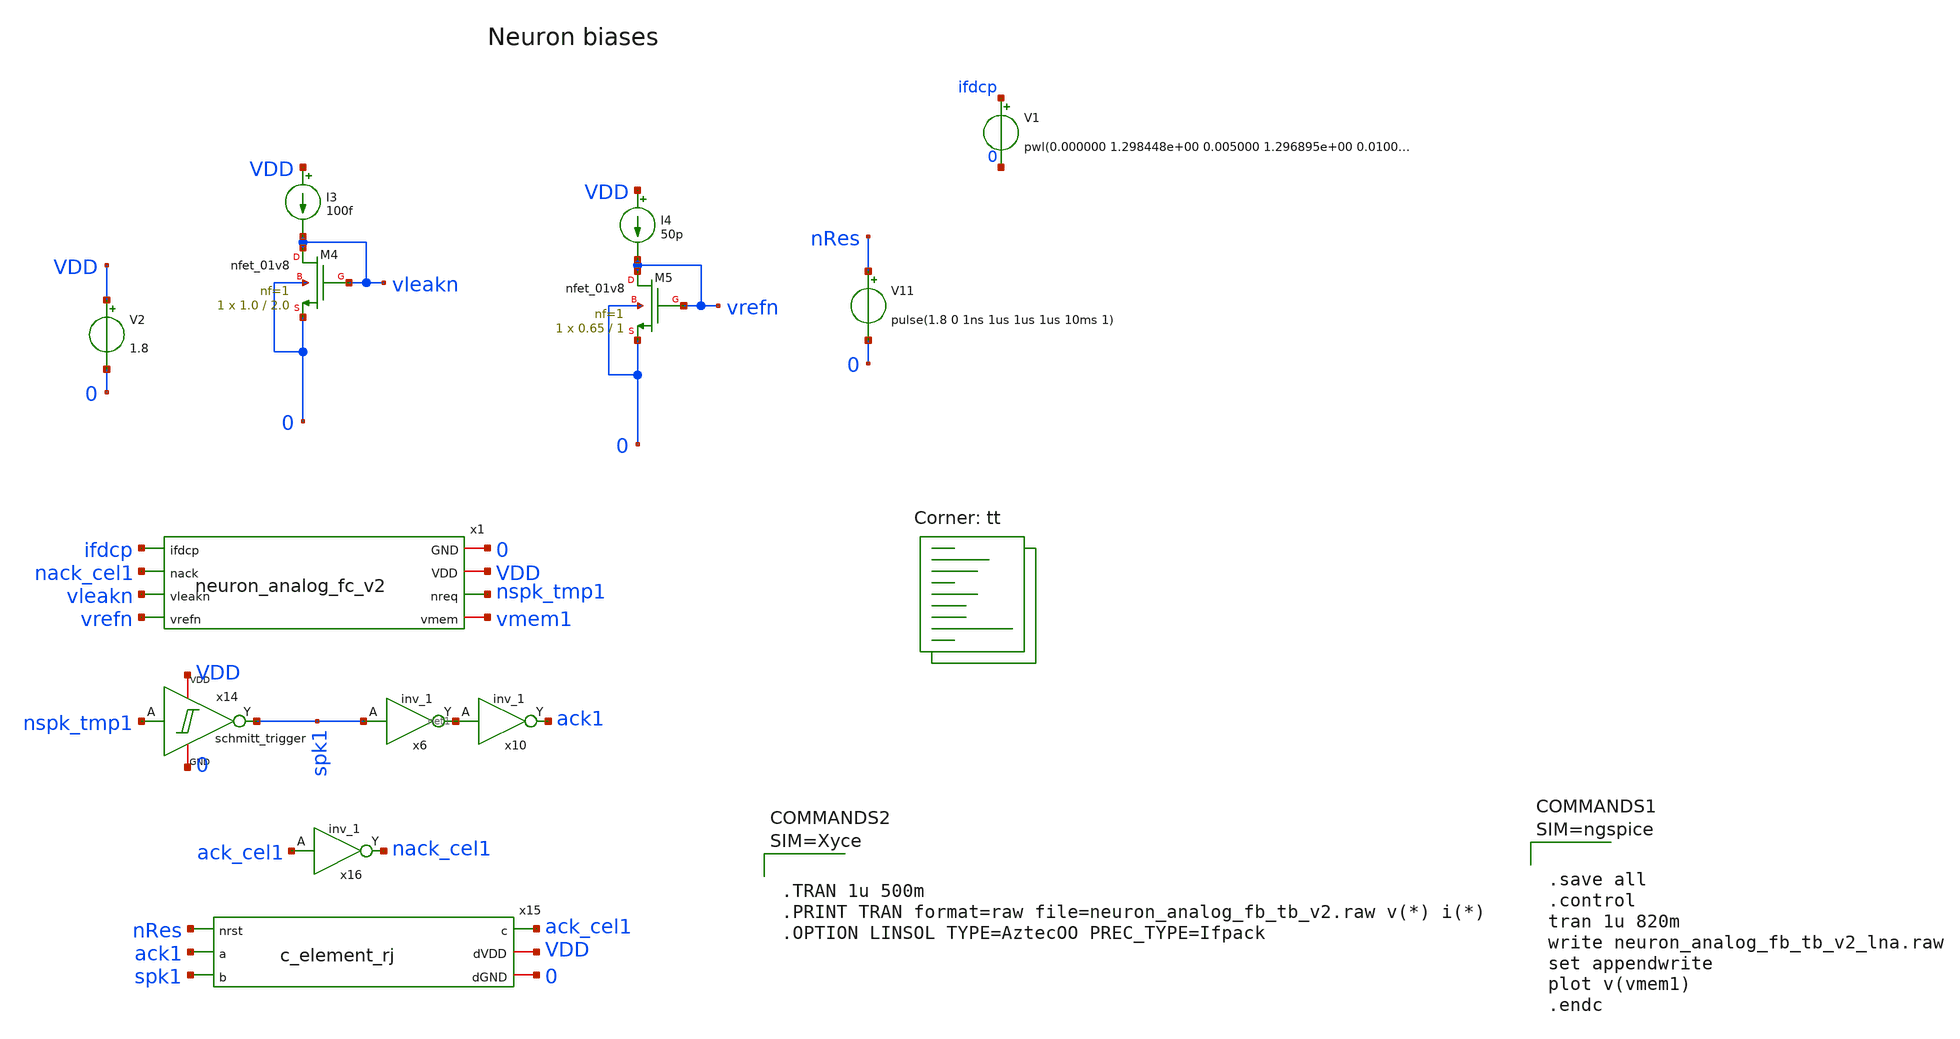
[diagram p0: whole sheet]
** sch_path: design/xschem/neuron_analog_fc_v2_tb_dc_lna.sch
**.subckt neuron_analog_fc_v2_tb_dc_lna
x1 0 VDD nspk_tmp1 ifdcp nack_cel1 vmem1 vleakn vrefn neuron_analog_fc_v2
V2 VDD 0 1.8
I3 VDD vleakn 100f
XM4 vleakn vleakn 0 0 sky130_fd_pr__nfet_01v8 L=2.0 W=1.0 nf=1 ad='int((nf+1)/2) * W/nf * 0.29' as='int((nf+2)/2) * W/nf * 0.29'
+ pd='2*int((nf+1)/2) * (W/nf + 0.29)' ps='2*int((nf+2)/2) * (W/nf + 0.29)' nrd='0.29 / W' nrs='0.29 / W'
+ sa=0 sb=0 sd=0 mult=1 m=1
I4 VDD vrefn 50p
XM5 vrefn vrefn 0 0 sky130_fd_pr__nfet_01v8 L=1 W=0.65 nf=1 ad='int((nf+1)/2) * W/nf * 0.29' as='int((nf+2)/2) * W/nf * 0.29'
+ pd='2*int((nf+1)/2) * (W/nf + 0.29)' ps='2*int((nf+2)/2) * (W/nf + 0.29)' nrd='0.29 / W' nrs='0.29 / W'
+ sa=0 sb=0 sd=0 mult=1 m=1
x16 ack_cel1 0 0 VDD VDD nack_cel1 sky130_fd_sc_hd__inv_1
x6 spk1 0 0 VDD VDD net1 sky130_fd_sc_hd__inv_1
x10 net1 0 0 VDD VDD ack1 sky130_fd_sc_hd__inv_1
x14 nspk_tmp1 spk1 VDD 0 schmitt_trigger
x15 nRes ack1 spk1 ack_cel1 VDD 0 c_element_rj
V11 nRes 0 pulse(1.8 0 1ns 1us 1us 1us 10ms 1)
V1 ifdcp 0 pwl(0.000000 1.298448e+00 0.005000 1.296895e+00 0.010000 1.303151e+00 0.015000
+ 1.301754e+00 0.020000 1.300714e+00 0.025000 1.301164e+00 0.030000 1.300912e+00 0.035000 1.299189e+00 0.040000
+ 1.302872e+00 0.045000 1.298281e+00 0.050000 1.300182e+00 0.055000 1.300439e+00 0.060000 1.300129e+00 0.065000
+ 1.299001e+00 0.070000 1.300924e+00 0.075000 1.297680e+00 0.080000 1.297533e+00 0.085000 1.299775e+00 0.090000
+ 1.298232e+00 0.095000 1.297533e+00 0.100000 1.297753e+00 0.105000 1.301787e+00 0.110000 1.298903e+00 0.115000
+ 1.299467e+00 0.120000 1.298675e+00 0.125000 1.297614e+00 0.130000 1.298554e+00 0.135000 1.299370e+00 0.140000
+ 1.302699e+00 0.145000 1.297011e+00 0.150000 1.299562e+00 0.155000 1.301264e+00 0.160000 1.296906e+00 0.165000
+ 1.300445e+00 0.170000 1.297892e+00 0.175000 1.301498e+00 0.180000 1.298067e+00 0.185000 1.297572e+00 0.190000
+ 1.299731e+00 0.195000 1.301248e+00 0.200000 1.299844e+00 0.205000 1.297327e+00 0.210000 1.299177e+00 0.215000
+ 1.301599e+00 0.220000 1.302386e+00 0.225000 1.298308e+00 0.230000 1.298810e+00 0.235000 1.299086e+00 0.240000
+ 1.301080e+00 0.245000 1.300521e+00 0.250000 1.300000e+00 0.255000 1.300038e+00 0.260000 1.295591e+00 0.265000
+ 1.280531e+00 0.270000 1.280815e+00 0.275000 1.274596e+00 0.280000 1.276162e+00 0.285000 1.273582e+00 0.290000
+ 1.272688e+00 0.295000 1.265704e+00 0.300000 1.264726e+00 0.305000 1.268659e+00 0.310000 1.266467e+00 0.315000
+ 1.264225e+00 0.320000 1.263942e+00 0.325000 1.261352e+00 0.330000 1.265376e+00 0.335000 1.258933e+00 0.340000
+ 1.261051e+00 0.345000 1.260239e+00 0.350000 1.263659e+00 0.355000 1.263858e+00 0.360000 1.267435e+00 0.365000
+ 1.269578e+00 0.370000 1.267600e+00 0.375000 1.267280e+00 0.380000 1.269908e+00 0.385000 1.272862e+00 0.390000
+ 1.266585e+00 0.395000 1.271646e+00 0.400000 1.271510e+00 0.405000 1.270244e+00 0.410000 1.263604e+00 0.415000
+ 1.267487e+00 0.420000 1.266101e+00 0.425000 1.272903e+00 0.430000 1.269502e+00 0.435000 1.265617e+00 0.440000
+ 1.262004e+00 0.445000 1.260263e+00 0.450000 1.262147e+00 0.455000 1.263582e+00 0.460000 1.264107e+00 0.465000
+ 1.264188e+00 0.470000 1.266783e+00 0.475000 1.269052e+00 0.480000 1.273404e+00 0.485000 1.277681e+00 0.490000
+ 1.272368e+00 0.495000 1.268262e+00 0.500000 1.270505e+00 0.505000 1.273283e+00 0.510000 1.270084e+00 0.515000
+ 1.273948e+00 0.520000 1.275330e+00 0.525000 1.277058e+00 0.530000 1.274241e+00 0.535000 1.269077e+00 0.540000
+ 1.270631e+00 0.545000 1.268163e+00 0.550000 1.270361e+00 0.555000 1.276698e+00 0.560000 1.278695e+00 0.565000
+ 1.298630e+00 0.570000 1.297646e+00 0.575000 1.297379e+00 0.580000 1.302470e+00 0.585000 1.297949e+00 0.590000
+ 1.300555e+00 0.595000 1.300788e+00 0.600000 1.296898e+00 0.605000 1.297809e+00 0.610000 1.301858e+00 0.615000
+ 1.301863e+00 0.620000 1.301843e+00 0.625000 1.300837e+00 0.630000 1.302801e+00 0.635000 1.299783e+00 0.640000
+ 1.302394e+00 0.645000 1.297782e+00 0.650000 1.302985e+00 0.655000 1.300231e+00 0.660000 1.299300e+00 0.665000
+ 1.299649e+00 0.670000 1.300673e+00 0.675000 1.300671e+00 0.680000 1.301464e+00 0.685000 1.300913e+00 0.690000
+ 1.299266e+00 0.695000 1.302546e+00 0.700000 1.302397e+00 0.705000 1.298858e+00 0.710000 1.299392e+00 0.715000
+ 1.301992e+00 0.720000 1.299221e+00 0.725000 1.300698e+00 0.730000 1.297068e+00 0.735000 1.300137e+00 0.740000
+ 1.299034e+00 0.745000 1.301633e+00 0.750000 1.298440e+00 0.755000 1.300146e+00 0.760000 1.300472e+00 0.765000
+ 1.298618e+00 0.770000 1.299711e+00 0.775000 1.301960e+00 0.780000 1.299843e+00 0.785000 1.299032e+00 0.790000
+ 1.303151e+00 0.795000 1.299843e+00 0.800000 1.302750e+00 0.805000 1.301839e+00 0.810000 1.300171e+00 0.815000
+ 1.302181e+00)
**** begin user architecture code



.save all
.control
tran 1u 820m
write neuron_analog_fb_tb_v2_lna.raw
set appendwrite
plot v(vmem1)
.endc



.lib $::SKYWATER_MODELS/sky130.lib.spice tt


* Standard cell simulation files
.include $::SKYWATER_STDCELLS/sky130_fd_sc_hd.spice




**** end user architecture code
**.ends

* expanding   symbol:  neuron_analog_fc_v2.sym # of pins=8
** sym_path: design/xschem/neuron_analog_fc_v2.sym
** sch_path: design/xschem/neuron_analog_fc_v2.sch
.subckt neuron_analog_fc_v2 GND VDD nreq ifdcp nack vmem vleakn vrefn
*.ipin vleakn
*.iopin GND
*.iopin VDD
*.opin nreq
*.ipin vrefn
*.ipin nack
*.ipin ifdcp
*.iopin vmem
XC1 GND vmem sky130_fd_pr__cap_mim_m3_1 W=5 L=5 MF=1 m=1
XM1 vmem ifdcp VDD VDD sky130_fd_pr__pfet_01v8 L=2.0 W=1.0 nf=1 ad='int((nf+1)/2) * W/nf * 0.29' as='int((nf+2)/2) * W/nf * 0.29'
+ pd='2*int((nf+1)/2) * (W/nf + 0.29)' ps='2*int((nf+2)/2) * (W/nf + 0.29)' nrd='0.29 / W' nrs='0.29 / W'
+ sa=0 sb=0 sd=0 mult=1 m=1
XM5 net2 nreq VDD VDD sky130_fd_pr__pfet_01v8 L=0.25 W=1.0 nf=1 ad='int((nf+1)/2) * W/nf * 0.29' as='int((nf+2)/2) * W/nf * 0.29'
+ pd='2*int((nf+1)/2) * (W/nf + 0.29)' ps='2*int((nf+2)/2) * (W/nf + 0.29)' nrd='0.29 / W' nrs='0.29 / W'
+ sa=0 sb=0 sd=0 mult=1 m=1
XM7 net3 nreq net4 GND sky130_fd_pr__nfet_01v8 L=0.15 W=0.6 nf=1 ad='int((nf+1)/2) * W/nf * 0.29' as='int((nf+2)/2) * W/nf * 0.29'
+ pd='2*int((nf+1)/2) * (W/nf + 0.29)' ps='2*int((nf+2)/2) * (W/nf + 0.29)' nrd='0.29 / W' nrs='0.29 / W'
+ sa=0 sb=0 sd=0 mult=1 m=1
XM6 net5 nack VDD VDD sky130_fd_pr__pfet_01v8 L=0.25 W=1.0 nf=1 ad='int((nf+1)/2) * W/nf * 0.29' as='int((nf+2)/2) * W/nf * 0.29'
+ pd='2*int((nf+1)/2) * (W/nf + 0.29)' ps='2*int((nf+2)/2) * (W/nf + 0.29)' nrd='0.29 / W' nrs='0.29 / W'
+ sa=0 sb=0 sd=0 mult=1 m=1
XM9 nreq vmem net2 VDD sky130_fd_pr__pfet_01v8 L=0.15 W=1.0 nf=1 ad='int((nf+1)/2) * W/nf * 0.29' as='int((nf+2)/2) * W/nf * 0.29'
+ pd='2*int((nf+1)/2) * (W/nf + 0.29)' ps='2*int((nf+2)/2) * (W/nf + 0.29)' nrd='0.29 / W' nrs='0.29 / W'
+ sa=0 sb=0 sd=0 mult=1 m=1
XM10 net3 nreq net5 VDD sky130_fd_pr__pfet_01v8 L=0.15 W=1.0 nf=1 ad='int((nf+1)/2) * W/nf * 0.29' as='int((nf+2)/2) * W/nf * 0.29'
+ pd='2*int((nf+1)/2) * (W/nf + 0.29)' ps='2*int((nf+2)/2) * (W/nf + 0.29)' nrd='0.29 / W' nrs='0.29 / W'
+ sa=0 sb=0 sd=0 mult=1 m=1
XM4 vmem nreq VDD VDD sky130_fd_pr__pfet_01v8 L=1.0 W=1.0 nf=1 ad='int((nf+1)/2) * W/nf * 0.29' as='int((nf+2)/2) * W/nf * 0.29'
+ pd='2*int((nf+1)/2) * (W/nf + 0.29)' ps='2*int((nf+2)/2) * (W/nf + 0.29)' nrd='0.29 / W' nrs='0.29 / W'
+ sa=0 sb=0 sd=0 mult=1 m=1
XM2 nreq vmem net1 GND sky130_fd_pr__nfet_01v8 L=0.15 W=0.6 nf=1 ad='int((nf+1)/2) * W/nf * 0.29' as='int((nf+2)/2) * W/nf * 0.29'
+ pd='2*int((nf+1)/2) * (W/nf + 0.29)' ps='2*int((nf+2)/2) * (W/nf + 0.29)' nrd='0.29 / W' nrs='0.29 / W'
+ sa=0 sb=0 sd=0 mult=1 m=1
XM3 net4 vrefn GND GND sky130_fd_pr__nfet_01v8 L=1.0 W=0.6 nf=1 ad='int((nf+1)/2) * W/nf * 0.29' as='int((nf+2)/2) * W/nf * 0.29'
+ pd='2*int((nf+1)/2) * (W/nf + 0.29)' ps='2*int((nf+2)/2) * (W/nf + 0.29)' nrd='0.29 / W' nrs='0.29 / W'
+ sa=0 sb=0 sd=0 mult=1 m=1
XM8 net1 net1 GND GND sky130_fd_pr__nfet_01v8 L=0.15 W=0.6 nf=1 ad='int((nf+1)/2) * W/nf * 0.29' as='int((nf+2)/2) * W/nf * 0.29'
+ pd='2*int((nf+1)/2) * (W/nf + 0.29)' ps='2*int((nf+2)/2) * (W/nf + 0.29)' nrd='0.29 / W' nrs='0.29 / W'
+ sa=0 sb=0 sd=0 mult=1 m=1
XM11 vmem net3 GND GND sky130_fd_pr__nfet_01v8 L=0.2 W=1.0 nf=1 ad='int((nf+1)/2) * W/nf * 0.29' as='int((nf+2)/2) * W/nf * 0.29'
+ pd='2*int((nf+1)/2) * (W/nf + 0.29)' ps='2*int((nf+2)/2) * (W/nf + 0.29)' nrd='0.29 / W' nrs='0.29 / W'
+ sa=0 sb=0 sd=0 mult=1 m=1
XM12 vmem vleakn GND GND sky130_fd_pr__nfet_01v8 L=2.0 W=1.0 nf=1 ad='int((nf+1)/2) * W/nf * 0.29' as='int((nf+2)/2) * W/nf * 0.29'
+ pd='2*int((nf+1)/2) * (W/nf + 0.29)' ps='2*int((nf+2)/2) * (W/nf + 0.29)' nrd='0.29 / W' nrs='0.29 / W'
+ sa=0 sb=0 sd=0 mult=1 m=1
XM13 GND net3 GND GND sky130_fd_pr__nfet_01v8 L=2.0 W=1.0 nf=1 ad='int((nf+1)/2) * W/nf * 0.29' as='int((nf+2)/2) * W/nf * 0.29'
+ pd='2*int((nf+1)/2) * (W/nf + 0.29)' ps='2*int((nf+2)/2) * (W/nf + 0.29)' nrd='0.29 / W' nrs='0.29 / W'
+ sa=0 sb=0 sd=0 mult=1 m=1
.ends


* expanding   symbol:  schmitt_trigger.sym # of pins=4
** sym_path: design/xschem/schmitt_trigger.sym
** sch_path: design/xschem/schmitt_trigger.sch
.subckt schmitt_trigger A Y VDD GND
*.ipin A
*.opin Y
*.iopin VDD
*.iopin GND
XM3 net2 A GND GND sky130_fd_pr__nfet_01v8 L=0.15 W=0.65 nf=1 ad='int((nf+1)/2) * W/nf * 0.29' as='int((nf+2)/2) * W/nf * 0.29'
+ pd='2*int((nf+1)/2) * (W/nf + 0.29)' ps='2*int((nf+2)/2) * (W/nf + 0.29)' nrd='0.29 / W' nrs='0.29 / W'
+ sa=0 sb=0 sd=0 mult=1 m=1
XM1 Y A net2 GND sky130_fd_pr__nfet_01v8 L=0.15 W=0.65 nf=1 ad='int((nf+1)/2) * W/nf * 0.29' as='int((nf+2)/2) * W/nf * 0.29'
+ pd='2*int((nf+1)/2) * (W/nf + 0.29)' ps='2*int((nf+2)/2) * (W/nf + 0.29)' nrd='0.29 / W' nrs='0.29 / W'
+ sa=0 sb=0 sd=0 mult=1 m=1
XM7 VDD Y net2 GND sky130_fd_pr__nfet_01v8 L=0.15 W=0.42 nf=1 ad='int((nf+1)/2) * W/nf * 0.29' as='int((nf+2)/2) * W/nf * 0.29'
+ pd='2*int((nf+1)/2) * (W/nf + 0.29)' ps='2*int((nf+2)/2) * (W/nf + 0.29)' nrd='0.29 / W' nrs='0.29 / W'
+ sa=0 sb=0 sd=0 mult=1 m=1
XM4 net1 A VDD VDD sky130_fd_pr__pfet_01v8 L=0.15 W=1 nf=1 ad='int((nf+1)/2) * W/nf * 0.29' as='int((nf+2)/2) * W/nf * 0.29'
+ pd='2*int((nf+1)/2) * (W/nf + 0.29)' ps='2*int((nf+2)/2) * (W/nf + 0.29)' nrd='0.29 / W' nrs='0.29 / W'
+ sa=0 sb=0 sd=0 mult=1 m=1
XM2 Y A net1 VDD sky130_fd_pr__pfet_01v8 L=0.15 W=1 nf=1 ad='int((nf+1)/2) * W/nf * 0.29' as='int((nf+2)/2) * W/nf * 0.29'
+ pd='2*int((nf+1)/2) * (W/nf + 0.29)' ps='2*int((nf+2)/2) * (W/nf + 0.29)' nrd='0.29 / W' nrs='0.29 / W'
+ sa=0 sb=0 sd=0 mult=1 m=1
XM5 GND Y net1 VDD sky130_fd_pr__pfet_01v8 L=0.15 W=0.82 nf=1 ad='int((nf+1)/2) * W/nf * 0.29' as='int((nf+2)/2) * W/nf * 0.29'
+ pd='2*int((nf+1)/2) * (W/nf + 0.29)' ps='2*int((nf+2)/2) * (W/nf + 0.29)' nrd='0.29 / W' nrs='0.29 / W'
+ sa=0 sb=0 sd=0 mult=1 m=1
.ends


* expanding   symbol:  c_element_rj.sym # of pins=6
** sym_path: design/xschem/c_element_rj.sym
** sch_path: design/xschem/c_element_rj.sch
.subckt c_element_rj nrst a b c dVDD dGND
*.iopin dGND
*.iopin dVDD
*.opin c
*.ipin b
*.ipin a
*.ipin nrst
XM14 c net6 dVDD dVDD sky130_fd_pr__pfet_01v8 L=0.15 W=1 nf=1 ad='int((nf+1)/2) * W/nf * 0.29' as='int((nf+2)/2) * W/nf * 0.29'
+ pd='2*int((nf+1)/2) * (W/nf + 0.29)' ps='2*int((nf+2)/2) * (W/nf + 0.29)' nrd='0.29 / W' nrs='0.29 / W'
+ sa=0 sb=0 sd=0 mult=1 m=1
XM5 net6 nrst dVDD dVDD sky130_fd_pr__pfet_01v8 L=0.15 W=1 nf=1 ad='int((nf+1)/2) * W/nf * 0.29' as='int((nf+2)/2) * W/nf * 0.29'
+ pd='2*int((nf+1)/2) * (W/nf + 0.29)' ps='2*int((nf+2)/2) * (W/nf + 0.29)' nrd='0.29 / W' nrs='0.29 / W'
+ sa=0 sb=0 sd=0 mult=1 m=1
XM6 net5 b dVDD dVDD sky130_fd_pr__pfet_01v8 L=0.15 W=1 nf=1 ad='int((nf+1)/2) * W/nf * 0.29' as='int((nf+2)/2) * W/nf * 0.29'
+ pd='2*int((nf+1)/2) * (W/nf + 0.29)' ps='2*int((nf+2)/2) * (W/nf + 0.29)' nrd='0.29 / W' nrs='0.29 / W'
+ sa=0 sb=0 sd=0 mult=1 m=1
XM4 net4 a dVDD dVDD sky130_fd_pr__pfet_01v8 L=0.15 W=1 nf=1 ad='int((nf+1)/2) * W/nf * 0.29' as='int((nf+2)/2) * W/nf * 0.29'
+ pd='2*int((nf+1)/2) * (W/nf + 0.29)' ps='2*int((nf+2)/2) * (W/nf + 0.29)' nrd='0.29 / W' nrs='0.29 / W'
+ sa=0 sb=0 sd=0 mult=1 m=1
XM7 net3 b net4 dVDD sky130_fd_pr__pfet_01v8 L=0.15 W=1 nf=1 ad='int((nf+1)/2) * W/nf * 0.29' as='int((nf+2)/2) * W/nf * 0.29'
+ pd='2*int((nf+1)/2) * (W/nf + 0.29)' ps='2*int((nf+2)/2) * (W/nf + 0.29)' nrd='0.29 / W' nrs='0.29 / W'
+ sa=0 sb=0 sd=0 mult=1 m=1
XM8 net3 a net5 dVDD sky130_fd_pr__pfet_01v8 L=0.15 W=1 nf=1 ad='int((nf+1)/2) * W/nf * 0.29' as='int((nf+2)/2) * W/nf * 0.29'
+ pd='2*int((nf+1)/2) * (W/nf + 0.29)' ps='2*int((nf+2)/2) * (W/nf + 0.29)' nrd='0.29 / W' nrs='0.29 / W'
+ sa=0 sb=0 sd=0 mult=1 m=1
XM10 net5 c net4 dVDD sky130_fd_pr__pfet_01v8 L=0.15 W=1 nf=1 ad='int((nf+1)/2) * W/nf * 0.29' as='int((nf+2)/2) * W/nf * 0.29'
+ pd='2*int((nf+1)/2) * (W/nf + 0.29)' ps='2*int((nf+2)/2) * (W/nf + 0.29)' nrd='0.29 / W' nrs='0.29 / W'
+ sa=0 sb=0 sd=0 mult=1 m=1
XM12 c net6 dGND dGND sky130_fd_pr__nfet_01v8 L=0.15 W=0.65 nf=1 ad='int((nf+1)/2) * W/nf * 0.29' as='int((nf+2)/2) * W/nf * 0.29'
+ pd='2*int((nf+1)/2) * (W/nf + 0.29)' ps='2*int((nf+2)/2) * (W/nf + 0.29)' nrd='0.29 / W' nrs='0.29 / W'
+ sa=0 sb=0 sd=0 mult=1 m=1
XM1 net3 nrst net6 dGND sky130_fd_pr__nfet_01v8 L=0.15 W=0.65 nf=1 ad='int((nf+1)/2) * W/nf * 0.29' as='int((nf+2)/2) * W/nf * 0.29'
+ pd='2*int((nf+1)/2) * (W/nf + 0.29)' ps='2*int((nf+2)/2) * (W/nf + 0.29)' nrd='0.29 / W' nrs='0.29 / W'
+ sa=0 sb=0 sd=0 mult=1 m=1
XM2 net3 b net1 dGND sky130_fd_pr__nfet_01v8 L=0.15 W=0.65 nf=1 ad='int((nf+1)/2) * W/nf * 0.29' as='int((nf+2)/2) * W/nf * 0.29'
+ pd='2*int((nf+1)/2) * (W/nf + 0.29)' ps='2*int((nf+2)/2) * (W/nf + 0.29)' nrd='0.29 / W' nrs='0.29 / W'
+ sa=0 sb=0 sd=0 mult=1 m=1
XM3 net3 a net2 dGND sky130_fd_pr__nfet_01v8 L=0.15 W=0.65 nf=1 ad='int((nf+1)/2) * W/nf * 0.29' as='int((nf+2)/2) * W/nf * 0.29'
+ pd='2*int((nf+1)/2) * (W/nf + 0.29)' ps='2*int((nf+2)/2) * (W/nf + 0.29)' nrd='0.29 / W' nrs='0.29 / W'
+ sa=0 sb=0 sd=0 mult=1 m=1
XM9 net2 c net1 dGND sky130_fd_pr__nfet_01v8 L=0.15 W=0.65 nf=1 ad='int((nf+1)/2) * W/nf * 0.29' as='int((nf+2)/2) * W/nf * 0.29'
+ pd='2*int((nf+1)/2) * (W/nf + 0.29)' ps='2*int((nf+2)/2) * (W/nf + 0.29)' nrd='0.29 / W' nrs='0.29 / W'
+ sa=0 sb=0 sd=0 mult=1 m=1
XM11 net1 a dGND dGND sky130_fd_pr__nfet_01v8 L=0.15 W=0.65 nf=1 ad='int((nf+1)/2) * W/nf * 0.29' as='int((nf+2)/2) * W/nf * 0.29'
+ pd='2*int((nf+1)/2) * (W/nf + 0.29)' ps='2*int((nf+2)/2) * (W/nf + 0.29)' nrd='0.29 / W' nrs='0.29 / W'
+ sa=0 sb=0 sd=0 mult=1 m=1
XM13 net2 b dGND dGND sky130_fd_pr__nfet_01v8 L=0.15 W=0.65 nf=1 ad='int((nf+1)/2) * W/nf * 0.29' as='int((nf+2)/2) * W/nf * 0.29'
+ pd='2*int((nf+1)/2) * (W/nf + 0.29)' ps='2*int((nf+2)/2) * (W/nf + 0.29)' nrd='0.29 / W' nrs='0.29 / W'
+ sa=0 sb=0 sd=0 mult=1 m=1
.ends

.end
